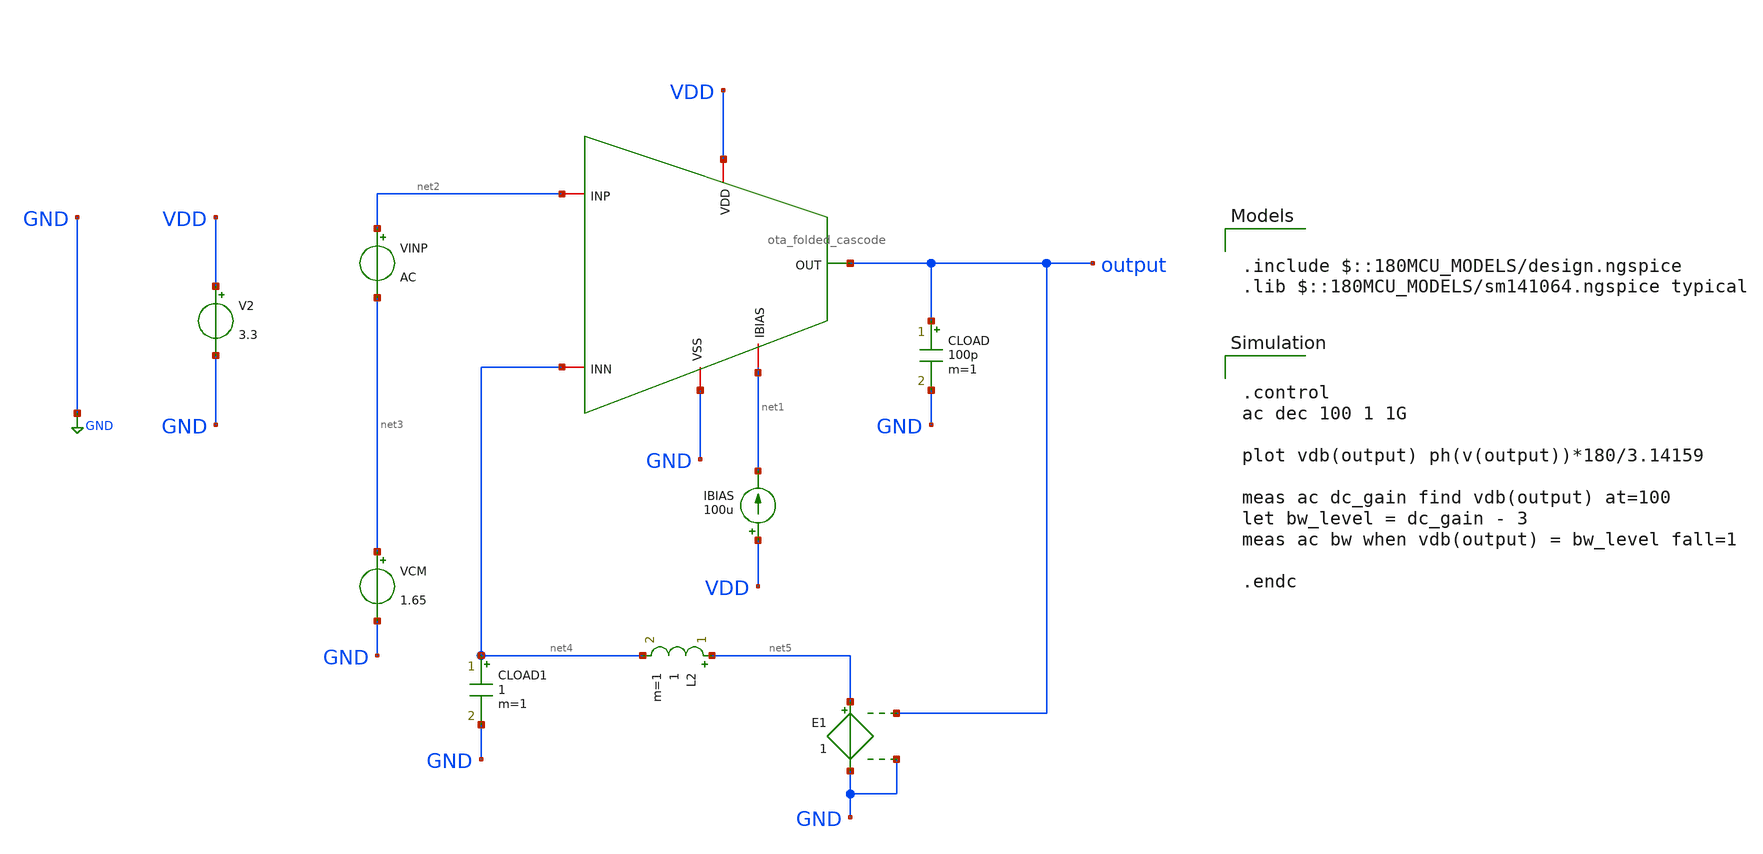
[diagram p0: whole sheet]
** sch_path: designs/libs/core_amps/ota_folded_cascode/ac_open_loop_tb.sch
**.subckt ac_open_loop_tb
IBIAS VDD net1 100u
V2 VDD GND 3.3
CLOAD output GND 100p m=1
VINP net2 net3 AC
VCM net3 GND 1.65
L2 net5 net4 1 m=1
CLOAD1 net4 GND 1 m=1
E1 net5 GND output GND 1
x1 VDD GND output net2 net4 net1 ota_folded_cascode
**** begin user architecture code

.include $::180MCU_MODELS/design.ngspice
.lib $::180MCU_MODELS/sm141064.ngspice typical



.control
ac dec 100 1 1G

plot vdb(output) ph(v(output))*180/3.14159

meas ac dc_gain find vdb(output) at=100
let bw_level = dc_gain - 3
meas ac bw when vdb(output) = bw_level fall=1

.endc



**** end user architecture code
**.ends
.GLOBAL GND
.end
